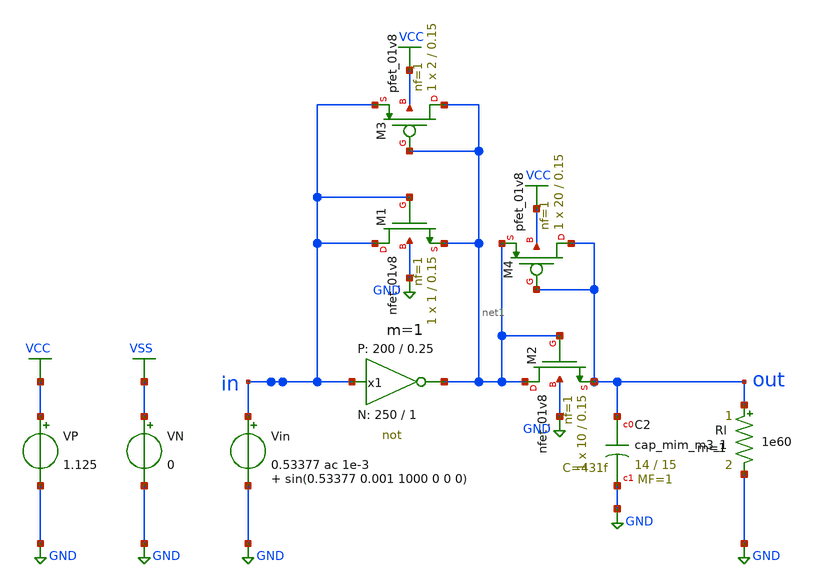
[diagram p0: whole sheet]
** sch_path: Amplifier_Inv/xschem/v2/DC_tb_v2.sch
* StefanSchippers/xschem_sky130/sky130_tests/not.sch:
* Copyright 2021 Stefan Frederik Schippers
* Licensed under the Apache License, Version 2.0 (the "License");
**.subckt DC_tb_v2
VN VSS GND 0
VP VCC GND 1.125
Vin in GND 0.53377 ac 1e-3 sin(0.53377 0.001 1000 0 0 0)
Rl out GND 1e60 m=1
x1 net1 in VCC VSS not W_N=250 L_N=1 W_P=200 L_P=0.25 m=1
XC2 out GND sky130_fd_pr__cap_mim_m3_1 W=14 L=15 MF=1 m=1
XM1 in in net1 GND sky130_fd_pr__nfet_01v8 L=0.15 W=1 nf=1 ad='int((nf+1)/2) * W/nf * 0.29' as='int((nf+2)/2) * W/nf * 0.29'
+ pd='2*int((nf+1)/2) * (W/nf + 0.29)' ps='2*int((nf+2)/2) * (W/nf + 0.29)' nrd='0.29 / W' nrs='0.29 / W'
+ sa=0 sb=0 sd=0 mult=1 m=1
XM3 net1 net1 in VCC sky130_fd_pr__pfet_01v8 L=0.15 W=2 nf=1 ad='int((nf+1)/2) * W/nf * 0.29' as='int((nf+2)/2) * W/nf * 0.29'
+ pd='2*int((nf+1)/2) * (W/nf + 0.29)' ps='2*int((nf+2)/2) * (W/nf + 0.29)' nrd='0.29 / W' nrs='0.29 / W'
+ sa=0 sb=0 sd=0 mult=1 m=1
XM2 net1 net1 out GND sky130_fd_pr__nfet_01v8 L=0.15 W=10 nf=1 ad='int((nf+1)/2) * W/nf * 0.29' as='int((nf+2)/2) * W/nf * 0.29'
+ pd='2*int((nf+1)/2) * (W/nf + 0.29)' ps='2*int((nf+2)/2) * (W/nf + 0.29)' nrd='0.29 / W' nrs='0.29 / W'
+ sa=0 sb=0 sd=0 mult=1 m=1
XM4 out out net1 VCC sky130_fd_pr__pfet_01v8 L=0.15 W=20 nf=1 ad='int((nf+1)/2) * W/nf * 0.29' as='int((nf+2)/2) * W/nf * 0.29'
+ pd='2*int((nf+1)/2) * (W/nf + 0.29)' ps='2*int((nf+2)/2) * (W/nf + 0.29)' nrd='0.29 / W' nrs='0.29 / W'
+ sa=0 sb=0 sd=0 mult=1 m=1
**** begin user architecture code

** opencircuitdesign pdks install
.lib $::SKYWATER_MODELS/sky130.lib.spice tt



.control

  dc Vin 0 1.125 0.00001
  save all v(out) v(in)
  write tb_inv_sky130_a_DC_v2.raw v(out) v(in)

.endc


**** end user architecture code
**.ends

* expanding   symbol:  sky130_tests/not.sym # of pins=2
** sym_path: sky130_tests/not.sym
** sch_path: sky130_tests/not.sch
.subckt not y a VCCPIN VSSPIN     W_N=1 L_N=0.15 W_P=2 L_P=0.15
*.opin y
*.ipin a
XM1 DN a VSSPIN VSSPIN sky130_fd_pr__nfet_01v8 L=L_N W=W_N nf=1 ad='int((1 + 1)/2) * W_N / 1 * 0.29'
+ as='int((1 + 2)/2) * W_N / 1 * 0.29' pd='2*int((1 + 1)/2) * (W_N / 1 + 0.29)' ps='2*int((1 + 2)/2) * (W_N / 1 + 0.29)'
+ nrd='0.29 / W_N ' nrs='0.29 / W_N ' sa=0 sb=0 sd=0 mult=1 m=1
XM2 DP a VCCPIN VCCPIN sky130_fd_pr__pfet_01v8 L=L_P W=W_P nf=1 ad='int((nf+1)/2) * W/nf * 0.29' as='int((nf+2)/2) * W/nf * 0.29'
+ pd='2*int((nf+1)/2) * (W/nf + 0.29)' ps='2*int((nf+2)/2) * (W/nf + 0.29)' nrd='0.29 / W' nrs='0.29 / W'
+ sa=0 sb=0 sd=0 mult=1 m=1
Vmeas DP y 0
.save i(vmeas)
Vmeas1 y DN 0
.save i(vmeas1)
.save v(dp)
.save v(dn)
.ends

.GLOBAL GND
.GLOBAL VSS
.GLOBAL VCC
.end
